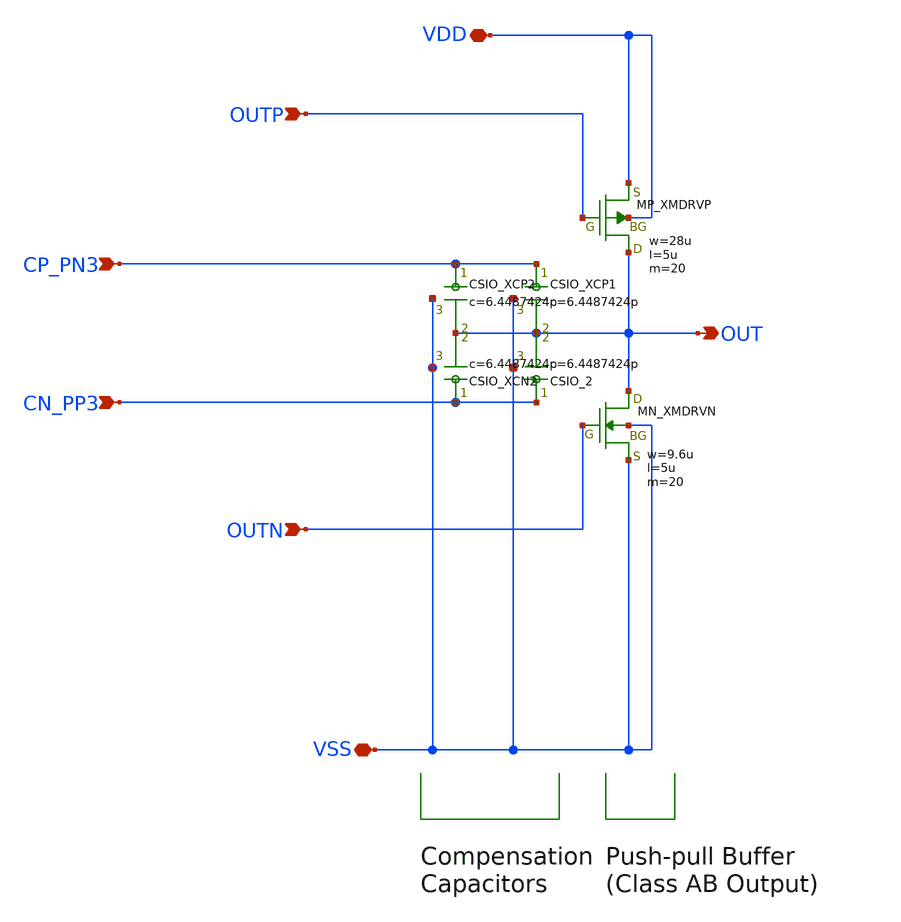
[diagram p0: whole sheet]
** sch_path: member_project/opamp_r2r_audio/3zki/opamp_3zki_R06_2V5_2.sch
**.subckt opamp_3zki_R06_2V5_2 VDD VSS OUT OUTP OUTN CP_PN3 CN_PP3
*.iopin VDD
*.iopin VSS
*.opin OUT
*.ipin OUTP
*.ipin OUTN
*.ipin CP_PN3
*.ipin CN_PP3
XMDRVP OUT OUTP VDD VDD PMOS w=28u l=5u as=21p ad=21p ps=17u pd=17u nrd=0 nrs=0 m=20
XMDRVN OUT OUTN VSS VSS NMOS w=9.6u l=5u as=7.2p ad=7.2p ps=7.8u pd=7.8u nrd=0 nrs=0 m=20
XCP1 CP_PN3 OUT VSS F_CSIO c=6.4487424p x=120u y=87.3u m=1
XCP2 CP_PN3 OUT VSS F_CSIO c=6.4487424p x=120u y=87.3u m=1
2 CN_PP3 OUT VSS F_CSIO c=6.4487424p x=120u y=87.3u m=1
XCN2 CN_PP3 OUT VSS F_CSIO c=6.4487424p x=120u y=87.3u m=1
**.ends
.end
